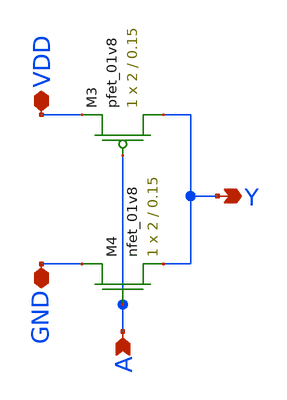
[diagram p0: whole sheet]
** sch_path: schematic/layout_driven_schematics/inverter.sch
**.subckt inverter A VDD GND Y
*.ipin A
*.iopin VDD
*.iopin GND
*.opin Y
XM3 Y A VDD VDD sky130_fd_pr__pfet_01v8 L=0.15 W=2 nf=1 ad='int((nf+1)/2) * W/nf * 0.29' as='int((nf+2)/2) * W/nf * 0.29'
+ pd='2*int((nf+1)/2) * (W/nf + 0.29)' ps='2*int((nf+2)/2) * (W/nf + 0.29)' nrd='0.29 / W' nrs='0.29 / W'
+ sa=0 sb=0 sd=0 mult=1 m=1
XM4 GND A Y GND sky130_fd_pr__nfet_01v8 L=0.15 W=2 nf=1 ad='int((nf+1)/2) * W/nf * 0.29' as='int((nf+2)/2) * W/nf * 0.29'
+ pd='2*int((nf+1)/2) * (W/nf + 0.29)' ps='2*int((nf+2)/2) * (W/nf + 0.29)' nrd='0.29 / W' nrs='0.29 / W'
+ sa=0 sb=0 sd=0 mult=1 m=1
**.ends
.end
